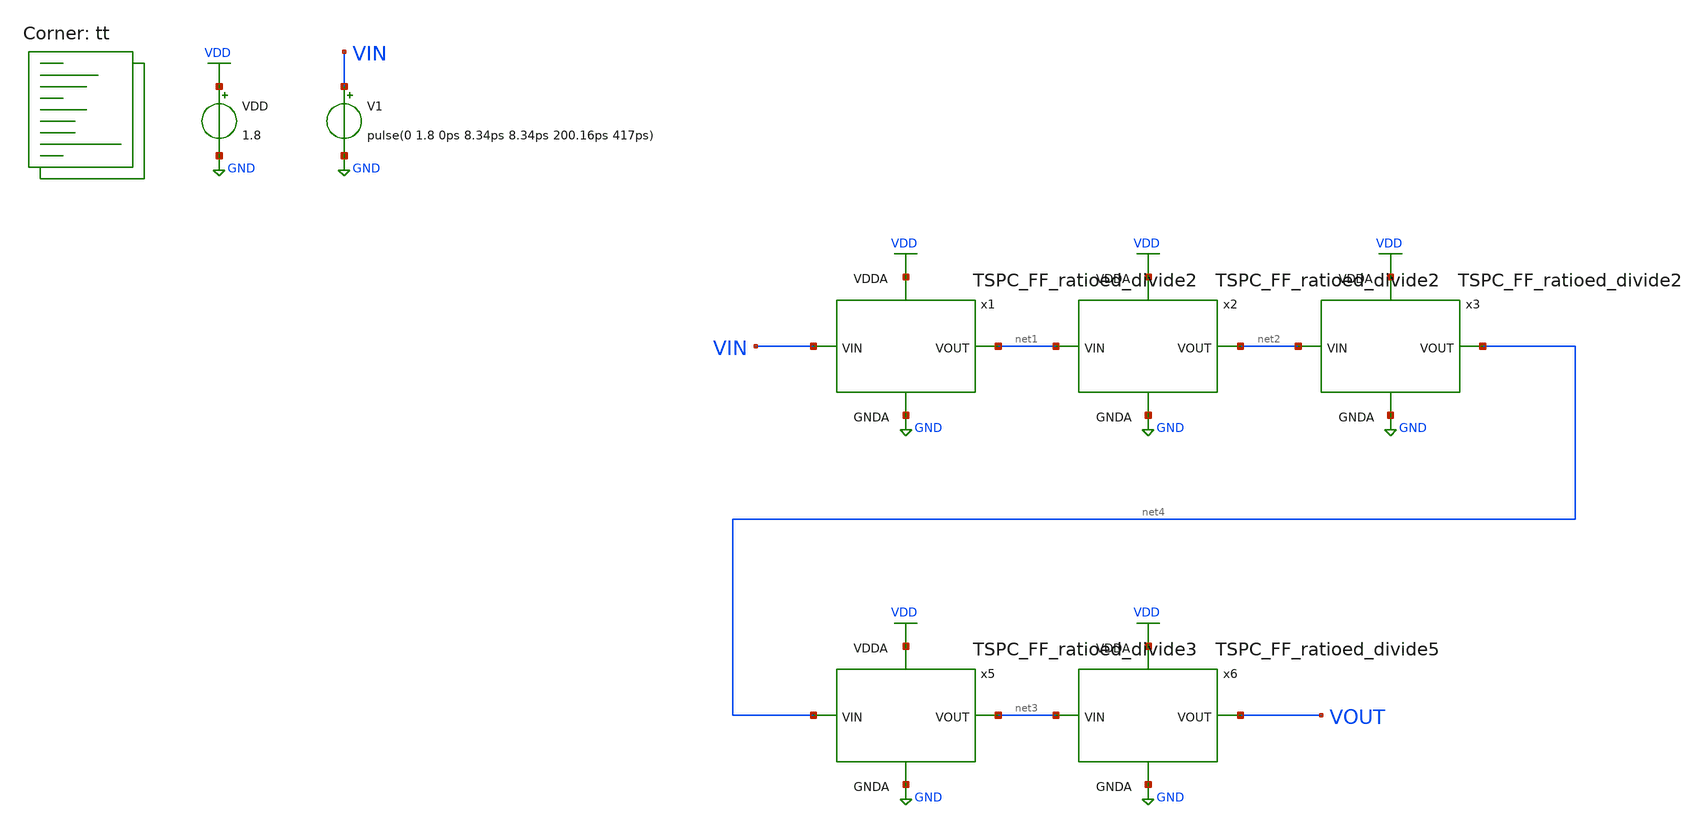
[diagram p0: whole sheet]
** sch_path: projects/pll/divider/xschem_ngspice/tb_TSPC_FF_ratioed_divide120.sch
**.subckt tb_TSPC_FF_ratioed_divide120
VDD VDD GND 1.8
V1 VIN GND pulse(0 1.8 0ps 8.34ps 8.34ps 200.16ps 417ps)
x1 net1 VIN VDD GND TSPC_FF_ratioed_divide2
x2 net2 net1 VDD GND TSPC_FF_ratioed_divide2
x3 net4 net2 VDD GND TSPC_FF_ratioed_divide2
x5 net3 net4 VDD GND TSPC_FF_ratioed_divide3
x6 VOUT net3 VDD GND TSPC_FF_ratioed_divide5
**** begin user architecture code



.include /foss/pdks/sky130A/libs.ref/sky130_fd_sc_hd/spice/sky130_fd_sc_hd.spice

.option method=gear
.option wnflag=1
* .option savecurrents


*.ic v(d)=0
*.ic v(q)=0
*.ic v(q1)=0

.probe p(x1)

.control

  save v(vin) v(vout) p(x1:power)
  * save v(vin) v(vout)
  * save all
  * tran 0.1n 1u
  tran 10p 0.5u

  remzerovec
  write tb_TSPC_FF_ratioed_divide120.raw
  * set appendwrite

.endc



.lib $::SKYWATER_MODELS/sky130.lib.spice tt
**** end user architecture code
**.ends

* expanding   symbol:
*+  /foss/designs/my_design/projects/pll/divider/xschem_ngspice/TSPC_FF_ratioed_divide2.sym # of pins=4
** sym_path: projects/pll/divider/xschem_ngspice/TSPC_FF_ratioed_divide2.sym
** sch_path: projects/pll/divider/xschem_ngspice/TSPC_FF_ratioed_divide2.sch
.subckt TSPC_FF_ratioed_divide2 VOUT VIN VDDA GNDA
*.ipin VIN
*.opin VOUT
*.ipin VDDA
*.ipin GNDA
XM24 VOUT VIN VDDA VDDA sky130_fd_pr__pfet_01v8 L=0.15 W=0.43 nf=1 ad='int((nf+1)/2) * W/nf * 0.29' as='int((nf+2)/2) * W/nf * 0.29'
+ pd='2*int((nf+1)/2) * (W/nf + 0.29)' ps='2*int((nf+2)/2) * (W/nf + 0.29)' nrd='0.29 / W' nrs='0.29 / W'
+ sa=0 sb=0 sd=0 mult=1 m=1
XM29 VOUT net1 GNDA GNDA sky130_fd_pr__nfet_01v8 L=0.15 W=0.43 nf=1 ad='int((nf+1)/2) * W/nf * 0.29'
+ as='int((nf+2)/2) * W/nf * 0.29' pd='2*int((nf+1)/2) * (W/nf + 0.29)' ps='2*int((nf+2)/2) * (W/nf + 0.29)'
+ nrd='0.29 / W' nrs='0.29 / W' sa=0 sb=0 sd=0 mult=1 m=1
XM30 net1 net2 VDDA VDDA sky130_fd_pr__pfet_01v8 L=0.15 W=0.43 nf=1 ad='int((nf+1)/2) * W/nf * 0.29'
+ as='int((nf+2)/2) * W/nf * 0.29' pd='2*int((nf+1)/2) * (W/nf + 0.29)' ps='2*int((nf+2)/2) * (W/nf + 0.29)'
+ nrd='0.29 / W' nrs='0.29 / W' sa=0 sb=0 sd=0 mult=1 m=1
XM31 net1 VIN GNDA GNDA sky130_fd_pr__nfet_01v8 L=0.15 W=1.5 nf=1 ad='int((nf+1)/2) * W/nf * 0.29' as='int((nf+2)/2) * W/nf * 0.29'
+ pd='2*int((nf+1)/2) * (W/nf + 0.29)' ps='2*int((nf+2)/2) * (W/nf + 0.29)' nrd='0.29 / W' nrs='0.29 / W'
+ sa=0 sb=0 sd=0 mult=1 m=1
XM32 net2 VOUT VDDA VDDA sky130_fd_pr__pfet_01v8 L=0.15 W=0.43 nf=1 ad='int((nf+1)/2) * W/nf * 0.29'
+ as='int((nf+2)/2) * W/nf * 0.29' pd='2*int((nf+1)/2) * (W/nf + 0.29)' ps='2*int((nf+2)/2) * (W/nf + 0.29)'
+ nrd='0.29 / W' nrs='0.29 / W' sa=0 sb=0 sd=0 mult=1 m=1
XM33 net3 VOUT GNDA GNDA sky130_fd_pr__nfet_01v8 L=0.15 W=0.43 nf=1 ad='int((nf+1)/2) * W/nf * 0.29'
+ as='int((nf+2)/2) * W/nf * 0.29' pd='2*int((nf+1)/2) * (W/nf + 0.29)' ps='2*int((nf+2)/2) * (W/nf + 0.29)'
+ nrd='0.29 / W' nrs='0.29 / W' sa=0 sb=0 sd=0 mult=1 m=1
XM28 net2 VIN net3 GNDA sky130_fd_pr__nfet_01v8 L=0.15 W=0.43 nf=1 ad='int((nf+1)/2) * W/nf * 0.29' as='int((nf+2)/2) * W/nf * 0.29'
+ pd='2*int((nf+1)/2) * (W/nf + 0.29)' ps='2*int((nf+2)/2) * (W/nf + 0.29)' nrd='0.29 / W' nrs='0.29 / W'
+ sa=0 sb=0 sd=0 mult=1 m=1
.ends


* expanding   symbol:
*+  /foss/designs/my_design/projects/pll/divider/xschem_ngspice/TSPC_FF_ratioed_divide3.sym # of pins=4
** sym_path: projects/pll/divider/xschem_ngspice/TSPC_FF_ratioed_divide3.sym
** sch_path: projects/pll/divider/xschem_ngspice/TSPC_FF_ratioed_divide3.sch
.subckt TSPC_FF_ratioed_divide3 VOUT VIN VDDA GNDA
*.ipin VIN
*.opin VOUT
*.ipin VDDA
*.ipin GNDA
XM24 net7 VIN VDDA VDDA sky130_fd_pr__pfet_01v8 L=0.15 W=0.43 nf=1 ad='int((nf+1)/2) * W/nf * 0.29' as='int((nf+2)/2) * W/nf * 0.29'
+ pd='2*int((nf+1)/2) * (W/nf + 0.29)' ps='2*int((nf+2)/2) * (W/nf + 0.29)' nrd='0.29 / W' nrs='0.29 / W'
+ sa=0 sb=0 sd=0 mult=1 m=1
XM29 net7 net1 GNDA GNDA sky130_fd_pr__nfet_01v8 L=0.15 W=0.43 nf=1 ad='int((nf+1)/2) * W/nf * 0.29'
+ as='int((nf+2)/2) * W/nf * 0.29' pd='2*int((nf+1)/2) * (W/nf + 0.29)' ps='2*int((nf+2)/2) * (W/nf + 0.29)'
+ nrd='0.29 / W' nrs='0.29 / W' sa=0 sb=0 sd=0 mult=1 m=1
XM30 net1 net2 VDDA VDDA sky130_fd_pr__pfet_01v8 L=0.15 W=0.43 nf=1 ad='int((nf+1)/2) * W/nf * 0.29'
+ as='int((nf+2)/2) * W/nf * 0.29' pd='2*int((nf+1)/2) * (W/nf + 0.29)' ps='2*int((nf+2)/2) * (W/nf + 0.29)'
+ nrd='0.29 / W' nrs='0.29 / W' sa=0 sb=0 sd=0 mult=1 m=1
XM31 net1 VIN GNDA GNDA sky130_fd_pr__nfet_01v8 L=0.15 W=1.5 nf=1 ad='int((nf+1)/2) * W/nf * 0.29' as='int((nf+2)/2) * W/nf * 0.29'
+ pd='2*int((nf+1)/2) * (W/nf + 0.29)' ps='2*int((nf+2)/2) * (W/nf + 0.29)' nrd='0.29 / W' nrs='0.29 / W'
+ sa=0 sb=0 sd=0 mult=1 m=1
XM32 net2 VOUT VDDA VDDA sky130_fd_pr__pfet_01v8 L=0.15 W=0.43 nf=1 ad='int((nf+1)/2) * W/nf * 0.29'
+ as='int((nf+2)/2) * W/nf * 0.29' pd='2*int((nf+1)/2) * (W/nf + 0.29)' ps='2*int((nf+2)/2) * (W/nf + 0.29)'
+ nrd='0.29 / W' nrs='0.29 / W' sa=0 sb=0 sd=0 mult=1 m=1
XM33 net8 VOUT GNDA GNDA sky130_fd_pr__nfet_01v8 L=0.15 W=0.43 nf=1 ad='int((nf+1)/2) * W/nf * 0.29'
+ as='int((nf+2)/2) * W/nf * 0.29' pd='2*int((nf+1)/2) * (W/nf + 0.29)' ps='2*int((nf+2)/2) * (W/nf + 0.29)'
+ nrd='0.29 / W' nrs='0.29 / W' sa=0 sb=0 sd=0 mult=1 m=1
XM28 net2 VIN net8 GNDA sky130_fd_pr__nfet_01v8 L=0.15 W=0.43 nf=1 ad='int((nf+1)/2) * W/nf * 0.29' as='int((nf+2)/2) * W/nf * 0.29'
+ pd='2*int((nf+1)/2) * (W/nf + 0.29)' ps='2*int((nf+2)/2) * (W/nf + 0.29)' nrd='0.29 / W' nrs='0.29 / W'
+ sa=0 sb=0 sd=0 mult=1 m=1
XM34 net6 VIN VDDA VDDA sky130_fd_pr__pfet_01v8 L=0.15 W=0.43 nf=1 ad='int((nf+1)/2) * W/nf * 0.29' as='int((nf+2)/2) * W/nf * 0.29'
+ pd='2*int((nf+1)/2) * (W/nf + 0.29)' ps='2*int((nf+2)/2) * (W/nf + 0.29)' nrd='0.29 / W' nrs='0.29 / W'
+ sa=0 sb=0 sd=0 mult=1 m=1
XM39 net6 net4 GNDA GNDA sky130_fd_pr__nfet_01v8 L=0.15 W=0.43 nf=1 ad='int((nf+1)/2) * W/nf * 0.29'
+ as='int((nf+2)/2) * W/nf * 0.29' pd='2*int((nf+1)/2) * (W/nf + 0.29)' ps='2*int((nf+2)/2) * (W/nf + 0.29)'
+ nrd='0.29 / W' nrs='0.29 / W' sa=0 sb=0 sd=0 mult=1 m=1
XM40 net4 net5 VDDA VDDA sky130_fd_pr__pfet_01v8 L=0.15 W=0.43 nf=1 ad='int((nf+1)/2) * W/nf * 0.29'
+ as='int((nf+2)/2) * W/nf * 0.29' pd='2*int((nf+1)/2) * (W/nf + 0.29)' ps='2*int((nf+2)/2) * (W/nf + 0.29)'
+ nrd='0.29 / W' nrs='0.29 / W' sa=0 sb=0 sd=0 mult=1 m=1
XM41 net4 VIN GNDA GNDA sky130_fd_pr__nfet_01v8 L=0.15 W=1.5 nf=1 ad='int((nf+1)/2) * W/nf * 0.29' as='int((nf+2)/2) * W/nf * 0.29'
+ pd='2*int((nf+1)/2) * (W/nf + 0.29)' ps='2*int((nf+2)/2) * (W/nf + 0.29)' nrd='0.29 / W' nrs='0.29 / W'
+ sa=0 sb=0 sd=0 mult=1 m=1
XM42 net5 net6 VDDA VDDA sky130_fd_pr__pfet_01v8 L=0.15 W=0.43 nf=1 ad='int((nf+1)/2) * W/nf * 0.29'
+ as='int((nf+2)/2) * W/nf * 0.29' pd='2*int((nf+1)/2) * (W/nf + 0.29)' ps='2*int((nf+2)/2) * (W/nf + 0.29)'
+ nrd='0.29 / W' nrs='0.29 / W' sa=0 sb=0 sd=0 mult=1 m=1
XM43 net9 net7 net3 GNDA sky130_fd_pr__nfet_01v8 L=0.15 W=0.43 nf=1 ad='int((nf+1)/2) * W/nf * 0.29'
+ as='int((nf+2)/2) * W/nf * 0.29' pd='2*int((nf+1)/2) * (W/nf + 0.29)' ps='2*int((nf+2)/2) * (W/nf + 0.29)'
+ nrd='0.29 / W' nrs='0.29 / W' sa=0 sb=0 sd=0 mult=1 m=1
XM44 net5 VIN net9 GNDA sky130_fd_pr__nfet_01v8 L=0.15 W=0.43 nf=1 ad='int((nf+1)/2) * W/nf * 0.29' as='int((nf+2)/2) * W/nf * 0.29'
+ pd='2*int((nf+1)/2) * (W/nf + 0.29)' ps='2*int((nf+2)/2) * (W/nf + 0.29)' nrd='0.29 / W' nrs='0.29 / W'
+ sa=0 sb=0 sd=0 mult=1 m=1
XM4 VOUT net6 VDDA VDDA sky130_fd_pr__pfet_01v8 L=0.15 W=0.86 nf=2 ad='int((nf+1)/2) * W/nf * 0.29' as='int((nf+2)/2) * W/nf * 0.29'
+ pd='2*int((nf+1)/2) * (W/nf + 0.29)' ps='2*int((nf+2)/2) * (W/nf + 0.29)' nrd='0.29 / W' nrs='0.29 / W'
+ sa=0 sb=0 sd=0 mult=1 m=1
XM5 VOUT net6 GNDA GNDA sky130_fd_pr__nfet_01v8 L=0.15 W=0.43 nf=1 ad='int((nf+1)/2) * W/nf * 0.29' as='int((nf+2)/2) * W/nf * 0.29'
+ pd='2*int((nf+1)/2) * (W/nf + 0.29)' ps='2*int((nf+2)/2) * (W/nf + 0.29)' nrd='0.29 / W' nrs='0.29 / W'
+ sa=0 sb=0 sd=0 mult=1 m=1
XM6 net3 net6 GNDA GNDA sky130_fd_pr__nfet_01v8 L=0.15 W=0.43 nf=1 ad='int((nf+1)/2) * W/nf * 0.29' as='int((nf+2)/2) * W/nf * 0.29'
+ pd='2*int((nf+1)/2) * (W/nf + 0.29)' ps='2*int((nf+2)/2) * (W/nf + 0.29)' nrd='0.29 / W' nrs='0.29 / W'
+ sa=0 sb=0 sd=0 mult=1 m=1
XM7 net5 net7 VDDA VDDA sky130_fd_pr__pfet_01v8 L=0.15 W=0.43 nf=1 ad='int((nf+1)/2) * W/nf * 0.29' as='int((nf+2)/2) * W/nf * 0.29'
+ pd='2*int((nf+1)/2) * (W/nf + 0.29)' ps='2*int((nf+2)/2) * (W/nf + 0.29)' nrd='0.29 / W' nrs='0.29 / W'
+ sa=0 sb=0 sd=0 mult=1 m=1
.ends


* expanding   symbol:
*+  /foss/designs/my_design/projects/pll/divider/xschem_ngspice/TSPC_FF_ratioed_divide5.sym # of pins=4
** sym_path: projects/pll/divider/xschem_ngspice/TSPC_FF_ratioed_divide5.sym
** sch_path: projects/pll/divider/xschem_ngspice/TSPC_FF_ratioed_divide5.sch
.subckt TSPC_FF_ratioed_divide5 VOUT VIN VDDA GNDA
*.ipin VIN
*.opin VOUT
*.ipin VDDA
*.ipin GNDA
XM24 net11 VIN VDDA VDDA sky130_fd_pr__pfet_01v8 L=0.15 W=0.43 nf=1 ad='int((nf+1)/2) * W/nf * 0.29'
+ as='int((nf+2)/2) * W/nf * 0.29' pd='2*int((nf+1)/2) * (W/nf + 0.29)' ps='2*int((nf+2)/2) * (W/nf + 0.29)'
+ nrd='0.29 / W' nrs='0.29 / W' sa=0 sb=0 sd=0 mult=1 m=1
XM29 net11 net1 GNDA GNDA sky130_fd_pr__nfet_01v8 L=0.15 W=0.43 nf=1 ad='int((nf+1)/2) * W/nf * 0.29'
+ as='int((nf+2)/2) * W/nf * 0.29' pd='2*int((nf+1)/2) * (W/nf + 0.29)' ps='2*int((nf+2)/2) * (W/nf + 0.29)'
+ nrd='0.29 / W' nrs='0.29 / W' sa=0 sb=0 sd=0 mult=1 m=1
XM30 net1 net3 VDDA VDDA sky130_fd_pr__pfet_01v8 L=0.15 W=0.43 nf=1 ad='int((nf+1)/2) * W/nf * 0.29'
+ as='int((nf+2)/2) * W/nf * 0.29' pd='2*int((nf+1)/2) * (W/nf + 0.29)' ps='2*int((nf+2)/2) * (W/nf + 0.29)'
+ nrd='0.29 / W' nrs='0.29 / W' sa=0 sb=0 sd=0 mult=1 m=1
XM31 net1 VIN GNDA GNDA sky130_fd_pr__nfet_01v8 L=0.15 W=1.5 nf=1 ad='int((nf+1)/2) * W/nf * 0.29' as='int((nf+2)/2) * W/nf * 0.29'
+ pd='2*int((nf+1)/2) * (W/nf + 0.29)' ps='2*int((nf+2)/2) * (W/nf + 0.29)' nrd='0.29 / W' nrs='0.29 / W'
+ sa=0 sb=0 sd=0 mult=1 m=1
XM32 net3 net2 VDDA VDDA sky130_fd_pr__pfet_01v8 L=0.15 W=0.43 nf=1 ad='int((nf+1)/2) * W/nf * 0.29'
+ as='int((nf+2)/2) * W/nf * 0.29' pd='2*int((nf+1)/2) * (W/nf + 0.29)' ps='2*int((nf+2)/2) * (W/nf + 0.29)'
+ nrd='0.29 / W' nrs='0.29 / W' sa=0 sb=0 sd=0 mult=1 m=1
XM33 net12 net2 GNDA GNDA sky130_fd_pr__nfet_01v8 L=0.15 W=0.43 nf=1 ad='int((nf+1)/2) * W/nf * 0.29'
+ as='int((nf+2)/2) * W/nf * 0.29' pd='2*int((nf+1)/2) * (W/nf + 0.29)' ps='2*int((nf+2)/2) * (W/nf + 0.29)'
+ nrd='0.29 / W' nrs='0.29 / W' sa=0 sb=0 sd=0 mult=1 m=1
XM28 net3 VIN net12 GNDA sky130_fd_pr__nfet_01v8 L=0.15 W=0.43 nf=1 ad='int((nf+1)/2) * W/nf * 0.29'
+ as='int((nf+2)/2) * W/nf * 0.29' pd='2*int((nf+1)/2) * (W/nf + 0.29)' ps='2*int((nf+2)/2) * (W/nf + 0.29)'
+ nrd='0.29 / W' nrs='0.29 / W' sa=0 sb=0 sd=0 mult=1 m=1
XM34 net7 VIN VDDA VDDA sky130_fd_pr__pfet_01v8 L=0.15 W=0.43 nf=1 ad='int((nf+1)/2) * W/nf * 0.29' as='int((nf+2)/2) * W/nf * 0.29'
+ pd='2*int((nf+1)/2) * (W/nf + 0.29)' ps='2*int((nf+2)/2) * (W/nf + 0.29)' nrd='0.29 / W' nrs='0.29 / W'
+ sa=0 sb=0 sd=0 mult=1 m=1
XM39 net7 net5 GNDA GNDA sky130_fd_pr__nfet_01v8 L=0.15 W=0.43 nf=1 ad='int((nf+1)/2) * W/nf * 0.29'
+ as='int((nf+2)/2) * W/nf * 0.29' pd='2*int((nf+1)/2) * (W/nf + 0.29)' ps='2*int((nf+2)/2) * (W/nf + 0.29)'
+ nrd='0.29 / W' nrs='0.29 / W' sa=0 sb=0 sd=0 mult=1 m=1
XM40 net5 net6 VDDA VDDA sky130_fd_pr__pfet_01v8 L=0.15 W=0.43 nf=1 ad='int((nf+1)/2) * W/nf * 0.29'
+ as='int((nf+2)/2) * W/nf * 0.29' pd='2*int((nf+1)/2) * (W/nf + 0.29)' ps='2*int((nf+2)/2) * (W/nf + 0.29)'
+ nrd='0.29 / W' nrs='0.29 / W' sa=0 sb=0 sd=0 mult=1 m=1
XM41 net5 VIN GNDA GNDA sky130_fd_pr__nfet_01v8 L=0.15 W=1.5 nf=1 ad='int((nf+1)/2) * W/nf * 0.29' as='int((nf+2)/2) * W/nf * 0.29'
+ pd='2*int((nf+1)/2) * (W/nf + 0.29)' ps='2*int((nf+2)/2) * (W/nf + 0.29)' nrd='0.29 / W' nrs='0.29 / W'
+ sa=0 sb=0 sd=0 mult=1 m=1
XM42 net6 VOUT net8 VDDA sky130_fd_pr__pfet_01v8 L=0.15 W=0.43 nf=1 ad='int((nf+1)/2) * W/nf * 0.29'
+ as='int((nf+2)/2) * W/nf * 0.29' pd='2*int((nf+1)/2) * (W/nf + 0.29)' ps='2*int((nf+2)/2) * (W/nf + 0.29)'
+ nrd='0.29 / W' nrs='0.29 / W' sa=0 sb=0 sd=0 mult=1 m=1
XM43 net13 net7 net4 GNDA sky130_fd_pr__nfet_01v8 L=0.15 W=0.43 nf=1 ad='int((nf+1)/2) * W/nf * 0.29'
+ as='int((nf+2)/2) * W/nf * 0.29' pd='2*int((nf+1)/2) * (W/nf + 0.29)' ps='2*int((nf+2)/2) * (W/nf + 0.29)'
+ nrd='0.29 / W' nrs='0.29 / W' sa=0 sb=0 sd=0 mult=1 m=1
XM44 net6 VIN net13 GNDA sky130_fd_pr__nfet_01v8 L=0.15 W=0.43 nf=1 ad='int((nf+1)/2) * W/nf * 0.29'
+ as='int((nf+2)/2) * W/nf * 0.29' pd='2*int((nf+1)/2) * (W/nf + 0.29)' ps='2*int((nf+2)/2) * (W/nf + 0.29)'
+ nrd='0.29 / W' nrs='0.29 / W' sa=0 sb=0 sd=0 mult=1 m=1
XM4 net2 net7 VDDA VDDA sky130_fd_pr__pfet_01v8 L=0.15 W=0.86 nf=2 ad='int((nf+1)/2) * W/nf * 0.29' as='int((nf+2)/2) * W/nf * 0.29'
+ pd='2*int((nf+1)/2) * (W/nf + 0.29)' ps='2*int((nf+2)/2) * (W/nf + 0.29)' nrd='0.29 / W' nrs='0.29 / W'
+ sa=0 sb=0 sd=0 mult=1 m=1
XM5 net2 net7 GNDA GNDA sky130_fd_pr__nfet_01v8 L=0.15 W=0.43 nf=1 ad='int((nf+1)/2) * W/nf * 0.29' as='int((nf+2)/2) * W/nf * 0.29'
+ pd='2*int((nf+1)/2) * (W/nf + 0.29)' ps='2*int((nf+2)/2) * (W/nf + 0.29)' nrd='0.29 / W' nrs='0.29 / W'
+ sa=0 sb=0 sd=0 mult=1 m=1
XM6 net4 VOUT GNDA GNDA sky130_fd_pr__nfet_01v8 L=0.15 W=0.43 nf=1 ad='int((nf+1)/2) * W/nf * 0.29' as='int((nf+2)/2) * W/nf * 0.29'
+ pd='2*int((nf+1)/2) * (W/nf + 0.29)' ps='2*int((nf+2)/2) * (W/nf + 0.29)' nrd='0.29 / W' nrs='0.29 / W'
+ sa=0 sb=0 sd=0 mult=1 m=1
XM7 net6 net7 VDDA VDDA sky130_fd_pr__pfet_01v8 L=0.15 W=0.43 nf=1 ad='int((nf+1)/2) * W/nf * 0.29' as='int((nf+2)/2) * W/nf * 0.29'
+ pd='2*int((nf+1)/2) * (W/nf + 0.29)' ps='2*int((nf+2)/2) * (W/nf + 0.29)' nrd='0.29 / W' nrs='0.29 / W'
+ sa=0 sb=0 sd=0 mult=1 m=1
XM1 net8 net11 VDDA VDDA sky130_fd_pr__pfet_01v8 L=0.15 W=0.43 nf=1 ad='int((nf+1)/2) * W/nf * 0.29'
+ as='int((nf+2)/2) * W/nf * 0.29' pd='2*int((nf+1)/2) * (W/nf + 0.29)' ps='2*int((nf+2)/2) * (W/nf + 0.29)'
+ nrd='0.29 / W' nrs='0.29 / W' sa=0 sb=0 sd=0 mult=1 m=1
XM2 net4 net11 GNDA GNDA sky130_fd_pr__nfet_01v8 L=0.15 W=0.43 nf=1 ad='int((nf+1)/2) * W/nf * 0.29'
+ as='int((nf+2)/2) * W/nf * 0.29' pd='2*int((nf+1)/2) * (W/nf + 0.29)' ps='2*int((nf+2)/2) * (W/nf + 0.29)'
+ nrd='0.29 / W' nrs='0.29 / W' sa=0 sb=0 sd=0 mult=1 m=1
XM3 VOUT net7 VDDA VDDA sky130_fd_pr__pfet_01v8 L=0.15 W=0.43 nf=1 ad='int((nf+1)/2) * W/nf * 0.29' as='int((nf+2)/2) * W/nf * 0.29'
+ pd='2*int((nf+1)/2) * (W/nf + 0.29)' ps='2*int((nf+2)/2) * (W/nf + 0.29)' nrd='0.29 / W' nrs='0.29 / W'
+ sa=0 sb=0 sd=0 mult=1 m=1
XM8 VOUT net9 GNDA GNDA sky130_fd_pr__nfet_01v8 L=0.15 W=0.43 nf=1 ad='int((nf+1)/2) * W/nf * 0.29' as='int((nf+2)/2) * W/nf * 0.29'
+ pd='2*int((nf+1)/2) * (W/nf + 0.29)' ps='2*int((nf+2)/2) * (W/nf + 0.29)' nrd='0.29 / W' nrs='0.29 / W'
+ sa=0 sb=0 sd=0 mult=1 m=1
XM9 net9 net10 VDDA VDDA sky130_fd_pr__pfet_01v8 L=0.15 W=0.43 nf=1 ad='int((nf+1)/2) * W/nf * 0.29'
+ as='int((nf+2)/2) * W/nf * 0.29' pd='2*int((nf+1)/2) * (W/nf + 0.29)' ps='2*int((nf+2)/2) * (W/nf + 0.29)'
+ nrd='0.29 / W' nrs='0.29 / W' sa=0 sb=0 sd=0 mult=1 m=1
XM10 net9 net7 GNDA GNDA sky130_fd_pr__nfet_01v8 L=0.15 W=1.5 nf=1 ad='int((nf+1)/2) * W/nf * 0.29' as='int((nf+2)/2) * W/nf * 0.29'
+ pd='2*int((nf+1)/2) * (W/nf + 0.29)' ps='2*int((nf+2)/2) * (W/nf + 0.29)' nrd='0.29 / W' nrs='0.29 / W'
+ sa=0 sb=0 sd=0 mult=1 m=1
XM11 net10 VOUT VDDA VDDA sky130_fd_pr__pfet_01v8 L=0.15 W=0.43 nf=1 ad='int((nf+1)/2) * W/nf * 0.29'
+ as='int((nf+2)/2) * W/nf * 0.29' pd='2*int((nf+1)/2) * (W/nf + 0.29)' ps='2*int((nf+2)/2) * (W/nf + 0.29)'
+ nrd='0.29 / W' nrs='0.29 / W' sa=0 sb=0 sd=0 mult=1 m=1
XM12 net14 VOUT GNDA GNDA sky130_fd_pr__nfet_01v8 L=0.15 W=0.43 nf=1 ad='int((nf+1)/2) * W/nf * 0.29'
+ as='int((nf+2)/2) * W/nf * 0.29' pd='2*int((nf+1)/2) * (W/nf + 0.29)' ps='2*int((nf+2)/2) * (W/nf + 0.29)'
+ nrd='0.29 / W' nrs='0.29 / W' sa=0 sb=0 sd=0 mult=1 m=1
XM13 net10 net7 net14 GNDA sky130_fd_pr__nfet_01v8 L=0.15 W=0.43 nf=1 ad='int((nf+1)/2) * W/nf * 0.29'
+ as='int((nf+2)/2) * W/nf * 0.29' pd='2*int((nf+1)/2) * (W/nf + 0.29)' ps='2*int((nf+2)/2) * (W/nf + 0.29)'
+ nrd='0.29 / W' nrs='0.29 / W' sa=0 sb=0 sd=0 mult=1 m=1
.ends

.GLOBAL GND
.GLOBAL VDD
.end
